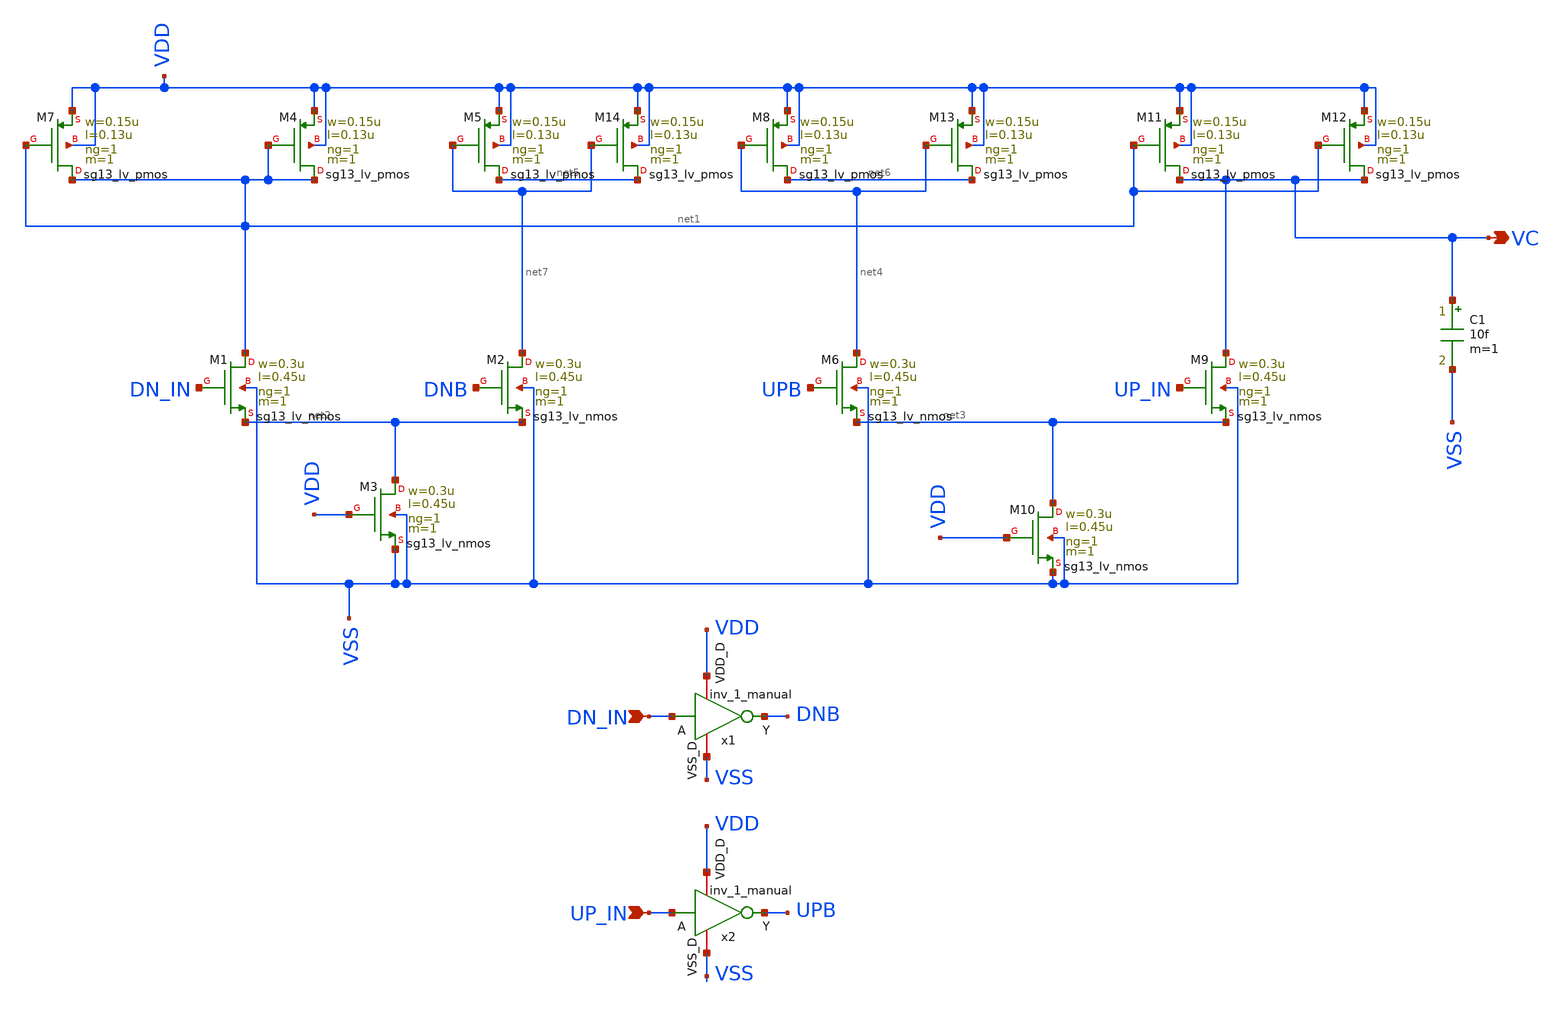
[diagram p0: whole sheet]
** sch_path: xschem/charge_pump/charge_pump.sch
**.subckt charge_pump VC UP_IN DN_IN
*.opin VC
*.ipin UP_IN
*.ipin DN_IN
XM1 net1 DN_IN net2 VSS sg13_lv_nmos w=0.3u l=0.45u ng=1 m=1 mm_ok=1
XM7 net1 net1 VDD VDD sg13_lv_pmos w=0.15u l=0.13u ng=1 m=1 mm_ok=1
XM2 net7 DNB net2 VSS sg13_lv_nmos w=0.3u l=0.45u ng=1 m=1 mm_ok=1
XM3 net2 VDD VSS VSS sg13_lv_nmos w=0.3u l=0.45u ng=1 m=1 mm_ok=1
XM4 net1 net1 VDD VDD sg13_lv_pmos w=0.15u l=0.13u ng=1 m=1 mm_ok=1
XM5 net5 net7 VDD VDD sg13_lv_pmos w=0.15u l=0.13u ng=1 m=1 mm_ok=1
XM6 net4 UPB net3 VSS sg13_lv_nmos w=0.3u l=0.45u ng=1 m=1 mm_ok=1
XM8 net6 net4 VDD VDD sg13_lv_pmos w=0.15u l=0.13u ng=1 m=1 mm_ok=1
XM9 VC UP_IN net3 VSS sg13_lv_nmos w=0.3u l=0.45u ng=1 m=1 mm_ok=1
XM10 net3 VDD VSS VSS sg13_lv_nmos w=0.3u l=0.45u ng=1 m=1 mm_ok=1
XM11 VC net1 VDD VDD sg13_lv_pmos w=0.15u l=0.13u ng=1 m=1 mm_ok=1
XM12 VC net1 VDD VDD sg13_lv_pmos w=0.15u l=0.13u ng=1 m=1 mm_ok=1
XM13 net6 net4 VDD VDD sg13_lv_pmos w=0.15u l=0.13u ng=1 m=1 mm_ok=1
XM14 net5 net7 VDD VDD sg13_lv_pmos w=0.15u l=0.13u ng=1 m=1 mm_ok=1
C1 VC VSS 10f m=1
x1 VDD DN_IN DNB VSS inv_1_manual
x2 VDD UP_IN UPB VSS inv_1_manual
**.ends

* expanding   symbol:  /foss/designs/UNIC-CASS-Aug25/sch/inv_1_manual/inv_1_manual.sym # of pins=4
** sym_path: xschem/inv_1_manual/inv_1_manual.sym
** sch_path: xschem/inv_1_manual/inv_1_manual.sch
.subckt inv_1_manual VDD_D A Y VSS_D
*.iopin VDD_D
*.iopin VSS_D
*.iopin A
*.iopin Y
XM1 Y A VSS_D VSS_D sg13_lv_nmos w=10u l=0.13u ng=1 m=1 mm_ok=1
XM2 Y A VDD_D VDD_D sg13_lv_pmos w=10u l=0.13u ng=1 m=1 mm_ok=1
.ends

.end
